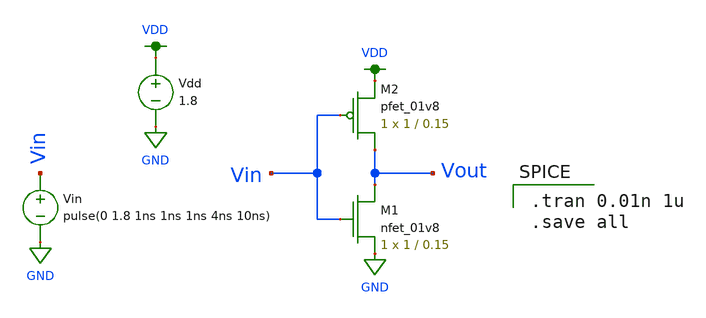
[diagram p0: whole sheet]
** sch_path: mp1/inverter/cmos_inverter_tran.sch
**.subckt cmos_inverter_tran
XM2 Vout Vin VDD VDD sky130_fd_pr__pfet_01v8 L=0.15 W=1 nf=1 ad='int((nf+1)/2) * W/nf * 0.29' as='int((nf+2)/2) * W/nf * 0.29'
+ pd='2*int((nf+1)/2) * (W/nf + 0.29)' ps='2*int((nf+2)/2) * (W/nf + 0.29)' nrd='0.29 / W' nrs='0.29 / W'
+ sa=0 sb=0 sd=0 mult=1 m=1
Vdd VDD GND 1.8
Vin Vin GND pulse(0 1.8 1ns 1ns 1ns 4ns 10ns)
XM1 Vout Vin GND GND sky130_fd_pr__nfet_01v8 L=0.15 W=1 nf=1 ad='int((nf+1)/2) * W/nf * 0.29' as='int((nf+2)/2) * W/nf * 0.29'
+ pd='2*int((nf+1)/2) * (W/nf + 0.29)' ps='2*int((nf+2)/2) * (W/nf + 0.29)' nrd='0.29 / W' nrs='0.29 / W'
+ sa=0 sb=0 sd=0 mult=1 m=1
**** begin user architecture code

.option wnflag=1
.lib ~/skywater/skywater-pdk/libraries/sky130_fd_pr_ngspice/latest/models/sky130.lib.spice tt


.tran 0.01n 1u
.save all

**** end user architecture code
**.ends
.GLOBAL VDD
.GLOBAL GND
.end
